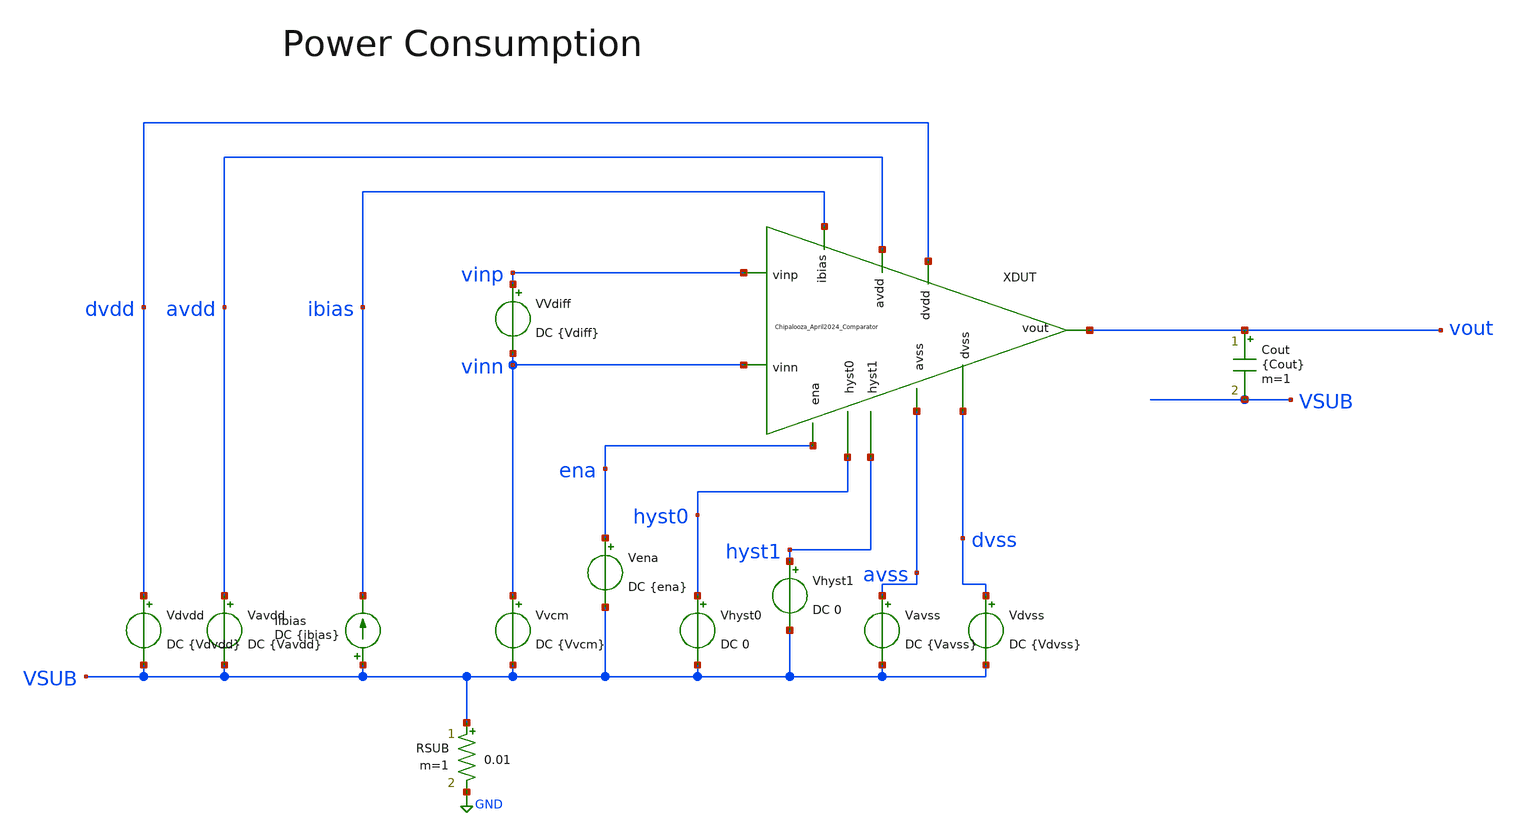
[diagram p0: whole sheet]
** sch_path: Chipalooza_April2024_Comparator/xschem/TB_powerConsumption.sch
**.subckt TB_powerConsumption
Vavdd avdd VSUB DC {Vavdd}
Cout vout VSUB {Cout} m=1
Vdvdd dvdd VSUB DC {Vdvdd}
Vvcm vinn VSUB DC {Vvcm}
Vena ena VSUB DC {ena}
Vhyst0 hyst0 VSUB DC 0
Vavss avss VSUB DC {Vavss}
Vdvss dvss VSUB DC {Vdvss}
RSUB VSUB GND 0.01 m=1
Iibias VSUB ibias DC {ibias}
VVdiff vinp vinn DC {Vdiff}
XDUT hyst0 hyst1 avdd vinp avss vinn dvdd dvss vout ibias ena Chipalooza_April2024_Comparator
Vhyst1 hyst1 VSUB DC 0
**** begin user architecture code

.control
.option savecurrents

.param vdvdd=1.8 vavdd=3.3 cout=1f
.param ibias=0.5u ena=1.8 Vhyst_0=1 Vhyst_1=1
.param vavss=0 vdvss=0
.param Vvcm=0 Vdiff=0.2


dc Vvcm 0 0.1 0.01
plot -(I(Vavdd) + I(Vdvdd)) + 500n

write TB_powerConsumption.raw

*quit

.endc


.lib $::SKYWATER_MODELS/sky130.lib.spice tt
**** end user architecture code
**.ends

* expanding   symbol:  Chipalooza_April2024_Comparator.sym # of pins=11
** sym_path: Chipalooza_April2024_Comparator/xschem/Chipalooza_April2024_Comparator.sym
** sch_path: Chipalooza_April2024_Comparator/xschem/Chipalooza_April2024_Comparator.sch
.subckt Chipalooza_April2024_Comparator hyst0 hyst1 avdd vinp avss vinn dvdd dvss vout ibias ena
*.ipin vinp
*.ipin vinn
*.ipin hyst0
*.ipin hyst1
*.ipin avdd
*.ipin avss
*.ipin dvdd
*.ipin dvss
*.opin vout
*.ipin ena
*.ipin ibias
XM29 SumOutBar SumOut dvdd dvdd sky130_fd_pr__pfet_01v8 L=1 W=2 nf=1 ad='int((nf+1)/2) * W/nf * 0.29'
+ as='int((nf+2)/2) * W/nf * 0.29' pd='2*int((nf+1)/2) * (W/nf + 0.29)' ps='2*int((nf+2)/2) * (W/nf + 0.29)'
+ nrd='0.29 / W' nrs='0.29 / W' sa=0 sb=0 sd=0 mult=2 m=2
XM30 SumOutBar SumOut avssi dvss sky130_fd_pr__nfet_01v8 L=1 W=2 nf=1 ad='int((nf+1)/2) * W/nf * 0.29'
+ as='int((nf+2)/2) * W/nf * 0.29' pd='2*int((nf+1)/2) * (W/nf + 0.29)' ps='2*int((nf+2)/2) * (W/nf + 0.29)'
+ nrd='0.29 / W' nrs='0.29 / W' sa=0 sb=0 sd=0 mult=2 m=2
XM25 net3 ibias avssi avss sky130_fd_pr__nfet_g5v0d10v5 L=1 W=1 nf=1 ad='int((nf+1)/2) * W/nf * 0.29'
+ as='int((nf+2)/2) * W/nf * 0.29' pd='2*int((nf+1)/2) * (W/nf + 0.29)' ps='2*int((nf+2)/2) * (W/nf + 0.29)'
+ nrd='0.29 / W' nrs='0.29 / W' sa=0 sb=0 sd=0 mult=2 m=2
C1 avss 0 2p m=1
XM38 avssi ena avss avss sky130_fd_pr__nfet_g5v0d10v5 L=1 W=32 nf=1 ad='int((nf+1)/2) * W/nf * 0.29'
+ as='int((nf+2)/2) * W/nf * 0.29' pd='2*int((nf+1)/2) * (W/nf + 0.29)' ps='2*int((nf+2)/2) * (W/nf + 0.29)'
+ nrd='0.29 / W' nrs='0.29 / W' sa=0 sb=0 sd=0 mult=8 m=8
XM39 net4 ibias avssi avss sky130_fd_pr__nfet_g5v0d10v5 L=1 W=3 nf=1 ad='int((nf+1)/2) * W/nf * 0.29'
+ as='int((nf+2)/2) * W/nf * 0.29' pd='2*int((nf+1)/2) * (W/nf + 0.29)' ps='2*int((nf+2)/2) * (W/nf + 0.29)'
+ nrd='0.29 / W' nrs='0.29 / W' sa=0 sb=0 sd=0 mult=2 m=2
XM16 vout SumOutBar dvdd dvdd sky130_fd_pr__pfet_01v8 L=1 W=2 nf=1 ad='int((nf+1)/2) * W/nf * 0.29' as='int((nf+2)/2) * W/nf * 0.29'
+ pd='2*int((nf+1)/2) * (W/nf + 0.29)' ps='2*int((nf+2)/2) * (W/nf + 0.29)' nrd='0.29 / W' nrs='0.29 / W'
+ sa=0 sb=0 sd=0 mult=2 m=2
XM18 vout SumOutBar avssi dvss sky130_fd_pr__nfet_01v8 L=1 W=2 nf=1 ad='int((nf+1)/2) * W/nf * 0.29'
+ as='int((nf+2)/2) * W/nf * 0.29' pd='2*int((nf+1)/2) * (W/nf + 0.29)' ps='2*int((nf+2)/2) * (W/nf + 0.29)'
+ nrd='0.29 / W' nrs='0.29 / W' sa=0 sb=0 sd=0 mult=2 m=2
XM4 SourceBias2 SourceBias2 avdd avdd sky130_fd_pr__pfet_g5v0d10v5 L=1 W=2 nf=1 ad='int((nf+1)/2) * W/nf * 0.29'
+ as='int((nf+2)/2) * W/nf * 0.29' pd='2*int((nf+1)/2) * (W/nf + 0.29)' ps='2*int((nf+2)/2) * (W/nf + 0.29)'
+ nrd='0.29 / W' nrs='0.29 / W' sa=0 sb=0 sd=0 mult=2 m=2
XM5 N1 SourceBias2 avdd avdd sky130_fd_pr__pfet_g5v0d10v5 L=1 W=2 nf=1 ad='int((nf+1)/2) * W/nf * 0.29'
+ as='int((nf+2)/2) * W/nf * 0.29' pd='2*int((nf+1)/2) * (W/nf + 0.29)' ps='2*int((nf+2)/2) * (W/nf + 0.29)'
+ nrd='0.29 / W' nrs='0.29 / W' sa=0 sb=0 sd=0 mult=2 m=2
XM6 N2 SourceBias2 avdd avdd sky130_fd_pr__pfet_g5v0d10v5 L=1 W=2 nf=1 ad='int((nf+1)/2) * W/nf * 0.29'
+ as='int((nf+2)/2) * W/nf * 0.29' pd='2*int((nf+1)/2) * (W/nf + 0.29)' ps='2*int((nf+2)/2) * (W/nf + 0.29)'
+ nrd='0.29 / W' nrs='0.29 / W' sa=0 sb=0 sd=0 mult=2 m=2
XM7 SumOut Bias1 N2 avdd sky130_fd_pr__pfet_g5v0d10v5 L=1 W=2 nf=1 ad='int((nf+1)/2) * W/nf * 0.29' as='int((nf+2)/2) * W/nf * 0.29'
+ pd='2*int((nf+1)/2) * (W/nf + 0.29)' ps='2*int((nf+2)/2) * (W/nf + 0.29)' nrd='0.29 / W' nrs='0.29 / W'
+ sa=0 sb=0 sd=0 mult=2 m=2
XM8 Sum Bias1 N1 avdd sky130_fd_pr__pfet_g5v0d10v5 L=1 W=2 nf=1 ad='int((nf+1)/2) * W/nf * 0.29' as='int((nf+2)/2) * W/nf * 0.29'
+ pd='2*int((nf+1)/2) * (W/nf + 0.29)' ps='2*int((nf+2)/2) * (W/nf + 0.29)' nrd='0.29 / W' nrs='0.29 / W'
+ sa=0 sb=0 sd=0 mult=2 m=2
XM9 SumOut Bias2 P2 avss sky130_fd_pr__nfet_g5v0d10v5 L=1 W=2 nf=1 ad='int((nf+1)/2) * W/nf * 0.29' as='int((nf+2)/2) * W/nf * 0.29'
+ pd='2*int((nf+1)/2) * (W/nf + 0.29)' ps='2*int((nf+2)/2) * (W/nf + 0.29)' nrd='0.29 / W' nrs='0.29 / W'
+ sa=0 sb=0 sd=0 mult=2 m=2
XM10 Sum Bias2 P1 avss sky130_fd_pr__nfet_g5v0d10v5 L=1 W=2 nf=1 ad='int((nf+1)/2) * W/nf * 0.29' as='int((nf+2)/2) * W/nf * 0.29'
+ pd='2*int((nf+1)/2) * (W/nf + 0.29)' ps='2*int((nf+2)/2) * (W/nf + 0.29)' nrd='0.29 / W' nrs='0.29 / W'
+ sa=0 sb=0 sd=0 mult=2 m=2
XM11 P2 Sum avssi avss sky130_fd_pr__nfet_g5v0d10v5 L=1 W=2 nf=1 ad='int((nf+1)/2) * W/nf * 0.29' as='int((nf+2)/2) * W/nf * 0.29'
+ pd='2*int((nf+1)/2) * (W/nf + 0.29)' ps='2*int((nf+2)/2) * (W/nf + 0.29)' nrd='0.29 / W' nrs='0.29 / W'
+ sa=0 sb=0 sd=0 mult=2 m=2
XM12 P1 Sum avssi avss sky130_fd_pr__nfet_g5v0d10v5 L=1 W=2 nf=1 ad='int((nf+1)/2) * W/nf * 0.29' as='int((nf+2)/2) * W/nf * 0.29'
+ pd='2*int((nf+1)/2) * (W/nf + 0.29)' ps='2*int((nf+2)/2) * (W/nf + 0.29)' nrd='0.29 / W' nrs='0.29 / W'
+ sa=0 sb=0 sd=0 mult=2 m=2
XM2 P2 vinn psource_input avdd sky130_fd_pr__pfet_g5v0d10v5 L=1 W=4 nf=1 ad='int((nf+1)/2) * W/nf * 0.29'
+ as='int((nf+2)/2) * W/nf * 0.29' pd='2*int((nf+1)/2) * (W/nf + 0.29)' ps='2*int((nf+2)/2) * (W/nf + 0.29)'
+ nrd='0.29 / W' nrs='0.29 / W' sa=0 sb=0 sd=0 mult=2 m=2
XM3 P1 vinp psource_input avdd sky130_fd_pr__pfet_g5v0d10v5 L=1 W=4 nf=1 ad='int((nf+1)/2) * W/nf * 0.29'
+ as='int((nf+2)/2) * W/nf * 0.29' pd='2*int((nf+1)/2) * (W/nf + 0.29)' ps='2*int((nf+2)/2) * (W/nf + 0.29)'
+ nrd='0.29 / W' nrs='0.29 / W' sa=0 sb=0 sd=0 mult=2 m=2
XM14 psource_input net5 avdd avdd sky130_fd_pr__pfet_g5v0d10v5 L=1 W=12 nf=1 ad='int((nf+1)/2) * W/nf * 0.29'
+ as='int((nf+2)/2) * W/nf * 0.29' pd='2*int((nf+1)/2) * (W/nf + 0.29)' ps='2*int((nf+2)/2) * (W/nf + 0.29)'
+ nrd='0.29 / W' nrs='0.29 / W' sa=0 sb=0 sd=0 mult=4 m=4
XM15 net5 net5 avdd avdd sky130_fd_pr__pfet_g5v0d10v5 L=1 W=8 nf=1 ad='int((nf+1)/2) * W/nf * 0.29' as='int((nf+2)/2) * W/nf * 0.29'
+ pd='2*int((nf+1)/2) * (W/nf + 0.29)' ps='2*int((nf+2)/2) * (W/nf + 0.29)' nrd='0.29 / W' nrs='0.29 / W'
+ sa=0 sb=0 sd=0 mult=2 m=2
XM17 nbias_tail net10 psource_input avdd sky130_fd_pr__pfet_g5v0d10v5 L=1 W=8 nf=1 ad='int((nf+1)/2) * W/nf * 0.29'
+ as='int((nf+2)/2) * W/nf * 0.29' pd='2*int((nf+1)/2) * (W/nf + 0.29)' ps='2*int((nf+2)/2) * (W/nf + 0.29)'
+ nrd='0.29 / W' nrs='0.29 / W' sa=0 sb=0 sd=0 mult=2 m=2
XM20 N1 vinp SourceBias0 avss sky130_fd_pr__nfet_g5v0d10v5 L=4 W=16 nf=1 ad='int((nf+1)/2) * W/nf * 0.29'
+ as='int((nf+2)/2) * W/nf * 0.29' pd='2*int((nf+1)/2) * (W/nf + 0.29)' ps='2*int((nf+2)/2) * (W/nf + 0.29)'
+ nrd='0.29 / W' nrs='0.29 / W' sa=0 sb=0 sd=0 mult=2 m=2
XM21 N2 vinn SourceBias0 avss sky130_fd_pr__nfet_g5v0d10v5 L=4 W=16 nf=1 ad='int((nf+1)/2) * W/nf * 0.29'
+ as='int((nf+2)/2) * W/nf * 0.29' pd='2*int((nf+1)/2) * (W/nf + 0.29)' ps='2*int((nf+2)/2) * (W/nf + 0.29)'
+ nrd='0.29 / W' nrs='0.29 / W' sa=0 sb=0 sd=0 mult=2 m=2
XM22 SourceBias0 nbias_tail avssi avss sky130_fd_pr__nfet_g5v0d10v5 L=1 W=12 nf=1 ad='int((nf+1)/2) * W/nf * 0.29'
+ as='int((nf+2)/2) * W/nf * 0.29' pd='2*int((nf+1)/2) * (W/nf + 0.29)' ps='2*int((nf+2)/2) * (W/nf + 0.29)'
+ nrd='0.29 / W' nrs='0.29 / W' sa=0 sb=0 sd=0 mult=4 m=4
XM23 nbias_tail nbias_tail avssi avss sky130_fd_pr__nfet_g5v0d10v5 L=1 W=12 nf=1 ad='int((nf+1)/2) * W/nf * 0.29'
+ as='int((nf+2)/2) * W/nf * 0.29' pd='2*int((nf+1)/2) * (W/nf + 0.29)' ps='2*int((nf+2)/2) * (W/nf + 0.29)'
+ nrd='0.29 / W' nrs='0.29 / W' sa=0 sb=0 sd=0 mult=2 m=2
XM28 net5 Bias5 SourceBias0 avss sky130_fd_pr__nfet_g5v0d10v5 L=1 W=4 nf=1 ad='int((nf+1)/2) * W/nf * 0.29'
+ as='int((nf+2)/2) * W/nf * 0.29' pd='2*int((nf+1)/2) * (W/nf + 0.29)' ps='2*int((nf+2)/2) * (W/nf + 0.29)'
+ nrd='0.29 / W' nrs='0.29 / W' sa=0 sb=0 sd=0 mult=2 m=2
XM45 SourceBias1 ibias avssi avss sky130_fd_pr__nfet_g5v0d10v5 L=1 W=3 nf=1 ad='int((nf+1)/2) * W/nf * 0.29'
+ as='int((nf+2)/2) * W/nf * 0.29' pd='2*int((nf+1)/2) * (W/nf + 0.29)' ps='2*int((nf+2)/2) * (W/nf + 0.29)'
+ nrd='0.29 / W' nrs='0.29 / W' sa=0 sb=0 sd=0 mult=2 m=2
XM46 SourceBias1 SourceBias1 avdd avdd sky130_fd_pr__pfet_g5v0d10v5 L=1 W=12 nf=1 ad='int((nf+1)/2) * W/nf * 0.29'
+ as='int((nf+2)/2) * W/nf * 0.29' pd='2*int((nf+1)/2) * (W/nf + 0.29)' ps='2*int((nf+2)/2) * (W/nf + 0.29)'
+ nrd='0.29 / W' nrs='0.29 / W' sa=0 sb=0 sd=0 mult=4 m=4
XM47 psource_input SourceBias1 avdd avdd sky130_fd_pr__pfet_g5v0d10v5 L=1 W=12 nf=1 ad='int((nf+1)/2) * W/nf * 0.29'
+ as='int((nf+2)/2) * W/nf * 0.29' pd='2*int((nf+1)/2) * (W/nf + 0.29)' ps='2*int((nf+2)/2) * (W/nf + 0.29)'
+ nrd='0.29 / W' nrs='0.29 / W' sa=0 sb=0 sd=0 mult=4 m=4
XM48 SourceBias2 ibias avssi avss sky130_fd_pr__nfet_g5v0d10v5 L=1 W=6 nf=1 ad='int((nf+1)/2) * W/nf * 0.29'
+ as='int((nf+2)/2) * W/nf * 0.29' pd='2*int((nf+1)/2) * (W/nf + 0.29)' ps='2*int((nf+2)/2) * (W/nf + 0.29)'
+ nrd='0.29 / W' nrs='0.29 / W' sa=0 sb=0 sd=0 mult=2 m=2
XM65 SourceBias3 ibias avssi avss sky130_fd_pr__nfet_g5v0d10v5 L=1 W=1 nf=1 ad='int((nf+1)/2) * W/nf * 0.29'
+ as='int((nf+2)/2) * W/nf * 0.29' pd='2*int((nf+1)/2) * (W/nf + 0.29)' ps='2*int((nf+2)/2) * (W/nf + 0.29)'
+ nrd='0.29 / W' nrs='0.29 / W' sa=0 sb=0 sd=0 mult=2 m=2
XM76 Bias1 ibias avssi avss sky130_fd_pr__nfet_g5v0d10v5 L=1 W=3 nf=1 ad='int((nf+1)/2) * W/nf * 0.29'
+ as='int((nf+2)/2) * W/nf * 0.29' pd='2*int((nf+1)/2) * (W/nf + 0.29)' ps='2*int((nf+2)/2) * (W/nf + 0.29)'
+ nrd='0.29 / W' nrs='0.29 / W' sa=0 sb=0 sd=0 mult=2 m=2
XM77 SourceBias5 ibias avssi avss sky130_fd_pr__nfet_g5v0d10v5 L=1 W=3 nf=1 ad='int((nf+1)/2) * W/nf * 0.29'
+ as='int((nf+2)/2) * W/nf * 0.29' pd='2*int((nf+1)/2) * (W/nf + 0.29)' ps='2*int((nf+2)/2) * (W/nf + 0.29)'
+ nrd='0.29 / W' nrs='0.29 / W' sa=0 sb=0 sd=0 mult=2 m=2
XM78 SourceBias6 ibias avssi avss sky130_fd_pr__nfet_g5v0d10v5 L=1 W=3 nf=1 ad='int((nf+1)/2) * W/nf * 0.29'
+ as='int((nf+2)/2) * W/nf * 0.29' pd='2*int((nf+1)/2) * (W/nf + 0.29)' ps='2*int((nf+2)/2) * (W/nf + 0.29)'
+ nrd='0.29 / W' nrs='0.29 / W' sa=0 sb=0 sd=0 mult=2 m=2
XM79 SourceBias7 ibias avssi avss sky130_fd_pr__nfet_g5v0d10v5 L=1 W=3 nf=1 ad='int((nf+1)/2) * W/nf * 0.29'
+ as='int((nf+2)/2) * W/nf * 0.29' pd='2*int((nf+1)/2) * (W/nf + 0.29)' ps='2*int((nf+2)/2) * (W/nf + 0.29)'
+ nrd='0.29 / W' nrs='0.29 / W' sa=0 sb=0 sd=0 mult=2 m=2
XM81 Bias5 ibias avssi avss sky130_fd_pr__nfet_g5v0d10v5 L=1 W=3 nf=1 ad='int((nf+1)/2) * W/nf * 0.29'
+ as='int((nf+2)/2) * W/nf * 0.29' pd='2*int((nf+1)/2) * (W/nf + 0.29)' ps='2*int((nf+2)/2) * (W/nf + 0.29)'
+ nrd='0.29 / W' nrs='0.29 / W' sa=0 sb=0 sd=0 mult=2 m=2
XM54 M55Source M55Drain avssi avss sky130_fd_pr__nfet_g5v0d10v5 L=1.5 W=6 nf=1 ad='int((nf+1)/2) * W/nf * 0.29'
+ as='int((nf+2)/2) * W/nf * 0.29' pd='2*int((nf+1)/2) * (W/nf + 0.29)' ps='2*int((nf+2)/2) * (W/nf + 0.29)'
+ nrd='0.29 / W' nrs='0.29 / W' sa=0 sb=0 sd=0 mult=2 m=2
XM55 M55Drain Bias2 M55Source avss sky130_fd_pr__nfet_g5v0d10v5 L=1 W=9 nf=1 ad='int((nf+1)/2) * W/nf * 0.29'
+ as='int((nf+2)/2) * W/nf * 0.29' pd='2*int((nf+1)/2) * (W/nf + 0.29)' ps='2*int((nf+2)/2) * (W/nf + 0.29)'
+ nrd='0.29 / W' nrs='0.29 / W' sa=0 sb=0 sd=0 mult=2 m=2
XM56 Bias2 Bias2 avssi avss sky130_fd_pr__nfet_g5v0d10v5 L=2 W=0.5 nf=1 ad='int((nf+1)/2) * W/nf * 0.29'
+ as='int((nf+2)/2) * W/nf * 0.29' pd='2*int((nf+1)/2) * (W/nf + 0.29)' ps='2*int((nf+2)/2) * (W/nf + 0.29)'
+ nrd='0.29 / W' nrs='0.29 / W' sa=0 sb=0 sd=0 mult=1 m=1
XM51 net6 net7 avdd avdd sky130_fd_pr__pfet_g5v0d10v5 L=2 W=20 nf=1 ad='int((nf+1)/2) * W/nf * 0.29'
+ as='int((nf+2)/2) * W/nf * 0.29' pd='2*int((nf+1)/2) * (W/nf + 0.29)' ps='2*int((nf+2)/2) * (W/nf + 0.29)'
+ nrd='0.29 / W' nrs='0.29 / W' sa=0 sb=0 sd=0 mult=2 m=2
XM49 net7 net7 avdd avdd sky130_fd_pr__pfet_g5v0d10v5 L=2 W=10 nf=1 ad='int((nf+1)/2) * W/nf * 0.29'
+ as='int((nf+2)/2) * W/nf * 0.29' pd='2*int((nf+1)/2) * (W/nf + 0.29)' ps='2*int((nf+2)/2) * (W/nf + 0.29)'
+ nrd='0.29 / W' nrs='0.29 / W' sa=0 sb=0 sd=0 mult=2 m=2
XM50 SourceBias4 SourceBias4 net7 avdd sky130_fd_pr__pfet_g5v0d10v5 L=1 W=10 nf=1 ad='int((nf+1)/2) * W/nf * 0.29'
+ as='int((nf+2)/2) * W/nf * 0.29' pd='2*int((nf+1)/2) * (W/nf + 0.29)' ps='2*int((nf+2)/2) * (W/nf + 0.29)'
+ nrd='0.29 / W' nrs='0.29 / W' sa=0 sb=0 sd=0 mult=2 m=2
XM52 avssi SourceBias4 net6 avdd sky130_fd_pr__pfet_g5v0d10v5 L=1 W=1 nf=1 ad='int((nf+1)/2) * W/nf * 0.29'
+ as='int((nf+2)/2) * W/nf * 0.29' pd='2*int((nf+1)/2) * (W/nf + 0.29)' ps='2*int((nf+2)/2) * (W/nf + 0.29)'
+ nrd='0.29 / W' nrs='0.29 / W' sa=0 sb=0 sd=0 mult=2 m=2
XM53 Bias1 Bias1 net6 avdd sky130_fd_pr__pfet_g5v0d10v5 L=1 W=10 nf=1 ad='int((nf+1)/2) * W/nf * 0.29'
+ as='int((nf+2)/2) * W/nf * 0.29' pd='2*int((nf+1)/2) * (W/nf + 0.29)' ps='2*int((nf+2)/2) * (W/nf + 0.29)'
+ nrd='0.29 / W' nrs='0.29 / W' sa=0 sb=0 sd=0 mult=2 m=2
XM66 net8 net9 avdd avdd sky130_fd_pr__pfet_g5v0d10v5 L=2 W=20 nf=1 ad='int((nf+1)/2) * W/nf * 0.29'
+ as='int((nf+2)/2) * W/nf * 0.29' pd='2*int((nf+1)/2) * (W/nf + 0.29)' ps='2*int((nf+2)/2) * (W/nf + 0.29)'
+ nrd='0.29 / W' nrs='0.29 / W' sa=0 sb=0 sd=0 mult=2 m=2
XM67 net9 net9 avdd avdd sky130_fd_pr__pfet_g5v0d10v5 L=2 W=20 nf=1 ad='int((nf+1)/2) * W/nf * 0.29'
+ as='int((nf+2)/2) * W/nf * 0.29' pd='2*int((nf+1)/2) * (W/nf + 0.29)' ps='2*int((nf+2)/2) * (W/nf + 0.29)'
+ nrd='0.29 / W' nrs='0.29 / W' sa=0 sb=0 sd=0 mult=2 m=2
XM68 SourceBias7 SourceBias7 net9 avdd sky130_fd_pr__pfet_g5v0d10v5 L=1 W=10 nf=1 ad='int((nf+1)/2) * W/nf * 0.29'
+ as='int((nf+2)/2) * W/nf * 0.29' pd='2*int((nf+1)/2) * (W/nf + 0.29)' ps='2*int((nf+2)/2) * (W/nf + 0.29)'
+ nrd='0.29 / W' nrs='0.29 / W' sa=0 sb=0 sd=0 mult=2 m=2
XM69 avssi SourceBias7 net8 avdd sky130_fd_pr__pfet_g5v0d10v5 L=1 W=1 nf=1 ad='int((nf+1)/2) * W/nf * 0.29'
+ as='int((nf+2)/2) * W/nf * 0.29' pd='2*int((nf+1)/2) * (W/nf + 0.29)' ps='2*int((nf+2)/2) * (W/nf + 0.29)'
+ nrd='0.29 / W' nrs='0.29 / W' sa=0 sb=0 sd=0 mult=2 m=2
XM70 Bias5 Bias5 net8 avdd sky130_fd_pr__pfet_g5v0d10v5 L=1 W=5 nf=1 ad='int((nf+1)/2) * W/nf * 0.29'
+ as='int((nf+2)/2) * W/nf * 0.29' pd='2*int((nf+1)/2) * (W/nf + 0.29)' ps='2*int((nf+2)/2) * (W/nf + 0.29)'
+ nrd='0.29 / W' nrs='0.29 / W' sa=0 sb=0 sd=0 mult=2 m=2
XM72 SourceBias5 SourceBias5 avdd avdd sky130_fd_pr__pfet_g5v0d10v5 L=1 W=12 nf=1 ad='int((nf+1)/2) * W/nf * 0.29'
+ as='int((nf+2)/2) * W/nf * 0.29' pd='2*int((nf+1)/2) * (W/nf + 0.29)' ps='2*int((nf+2)/2) * (W/nf + 0.29)'
+ nrd='0.29 / W' nrs='0.29 / W' sa=0 sb=0 sd=0 mult=4 m=4
XM73 M55Drain SourceBias5 avdd avdd sky130_fd_pr__pfet_g5v0d10v5 L=1 W=12 nf=1 ad='int((nf+1)/2) * W/nf * 0.29'
+ as='int((nf+2)/2) * W/nf * 0.29' pd='2*int((nf+1)/2) * (W/nf + 0.29)' ps='2*int((nf+2)/2) * (W/nf + 0.29)'
+ nrd='0.29 / W' nrs='0.29 / W' sa=0 sb=0 sd=0 mult=4 m=4
XM74 SourceBias6 SourceBias6 avdd avdd sky130_fd_pr__pfet_g5v0d10v5 L=1 W=12 nf=1 ad='int((nf+1)/2) * W/nf * 0.29'
+ as='int((nf+2)/2) * W/nf * 0.29' pd='2*int((nf+1)/2) * (W/nf + 0.29)' ps='2*int((nf+2)/2) * (W/nf + 0.29)'
+ nrd='0.29 / W' nrs='0.29 / W' sa=0 sb=0 sd=0 mult=4 m=4
XM75 Bias2 SourceBias6 avdd avdd sky130_fd_pr__pfet_g5v0d10v5 L=1 W=12 nf=1 ad='int((nf+1)/2) * W/nf * 0.29'
+ as='int((nf+2)/2) * W/nf * 0.29' pd='2*int((nf+1)/2) * (W/nf + 0.29)' ps='2*int((nf+2)/2) * (W/nf + 0.29)'
+ nrd='0.29 / W' nrs='0.29 / W' sa=0 sb=0 sd=0 mult=4 m=4
XM1 SourceBias0 ibias avssi avss sky130_fd_pr__nfet_g5v0d10v5 L=1 W=3 nf=1 ad='int((nf+1)/2) * W/nf * 0.29'
+ as='int((nf+2)/2) * W/nf * 0.29' pd='2*int((nf+1)/2) * (W/nf + 0.29)' ps='2*int((nf+2)/2) * (W/nf + 0.29)'
+ nrd='0.29 / W' nrs='0.29 / W' sa=0 sb=0 sd=0 mult=2 m=2
XM31 net1 hyst0 net3 avss sky130_fd_pr__nfet_01v8 L=1 W=1 nf=1 ad='int((1 + 1)/2) * 1 / 1 * 0.29' as='int((1 + 2)/2) * 1 / 1 * 0.29'
+ pd='2*int((1 + 1)/2) * (1 / 1 + 0.29)' ps='2*int((1 + 2)/2) * (1 / 1 + 0.29)' nrd='0.29 / 1 ' nrs='0.29 / 1 '
+ sa=0 sb=0 sd=0 mult=2 m=2
XM32 net1 hyst1 net4 avss sky130_fd_pr__nfet_01v8 L=1 W=3 nf=1 ad='int((1 + 1)/2) * 3 / 1 * 0.29' as='int((1 + 2)/2) * 3 / 1 * 0.29'
+ pd='2*int((1 + 1)/2) * (3 / 1 + 0.29)' ps='2*int((1 + 2)/2) * (3 / 1 + 0.29)' nrd='0.29 / 3 ' nrs='0.29 / 3 '
+ sa=0 sb=0 sd=0 mult=2 m=2
XM19 N1 SumOut net1 avss sky130_fd_pr__nfet_g5v0d10v5 L=1 W=2 nf=1 ad='int((nf+1)/2) * W/nf * 0.29' as='int((nf+2)/2) * W/nf * 0.29'
+ pd='2*int((nf+1)/2) * (W/nf + 0.29)' ps='2*int((nf+2)/2) * (W/nf + 0.29)' nrd='0.29 / W' nrs='0.29 / W'
+ sa=0 sb=0 sd=0 mult=2 m=2
XM24 N2 SumOutBar net1 avss sky130_fd_pr__nfet_g5v0d10v5 L=1 W=2 nf=1 ad='int((nf+1)/2) * W/nf * 0.29'
+ as='int((nf+2)/2) * W/nf * 0.29' pd='2*int((nf+1)/2) * (W/nf + 0.29)' ps='2*int((nf+2)/2) * (W/nf + 0.29)'
+ nrd='0.29 / W' nrs='0.29 / W' sa=0 sb=0 sd=0 mult=2 m=2
XM26 ibias ibias avssi avss sky130_fd_pr__nfet_g5v0d10v5 L=1 W=3 nf=1 ad='int((nf+1)/2) * W/nf * 0.29'
+ as='int((nf+2)/2) * W/nf * 0.29' pd='2*int((nf+1)/2) * (W/nf + 0.29)' ps='2*int((nf+2)/2) * (W/nf + 0.29)'
+ nrd='0.29 / W' nrs='0.29 / W' sa=0 sb=0 sd=0 mult=2 m=2
XM27 net2 ibias avssi avss sky130_fd_pr__nfet_g5v0d10v5 L=1 W=3 nf=1 ad='int((nf+1)/2) * W/nf * 0.29'
+ as='int((nf+2)/2) * W/nf * 0.29' pd='2*int((nf+1)/2) * (W/nf + 0.29)' ps='2*int((nf+2)/2) * (W/nf + 0.29)'
+ nrd='0.29 / W' nrs='0.29 / W' sa=0 sb=0 sd=0 mult=2 m=2
XM33 net2 net2 avdd avdd sky130_fd_pr__pfet_g5v0d10v5 L=1 W=3 nf=1 ad='int((nf+1)/2) * W/nf * 0.29' as='int((nf+2)/2) * W/nf * 0.29'
+ pd='2*int((nf+1)/2) * (W/nf + 0.29)' ps='2*int((nf+2)/2) * (W/nf + 0.29)' nrd='0.29 / W' nrs='0.29 / W'
+ sa=0 sb=0 sd=0 mult=2 m=2
XM34 avss net2 avdd avdd sky130_fd_pr__pfet_g5v0d10v5 L=1 W=3 nf=1 ad='int((nf+1)/2) * W/nf * 0.29' as='int((nf+2)/2) * W/nf * 0.29'
+ pd='2*int((nf+1)/2) * (W/nf + 0.29)' ps='2*int((nf+2)/2) * (W/nf + 0.29)' nrd='0.29 / W' nrs='0.29 / W'
+ sa=0 sb=0 sd=0 mult=2 m=2
XM63 net10 net10 avdd avdd sky130_fd_pr__pfet_g5v0d10v5 L=5 W=3 nf=1 ad='int((nf+1)/2) * W/nf * 0.29'
+ as='int((nf+2)/2) * W/nf * 0.29' pd='2*int((nf+1)/2) * (W/nf + 0.29)' ps='2*int((nf+2)/2) * (W/nf + 0.29)'
+ nrd='0.29 / W' nrs='0.29 / W' sa=0 sb=0 sd=0 mult=1 m=1
XM62 avdd Bias4 SourceBias3 avss sky130_fd_pr__nfet_g5v0d10v5 L=1 W=4 nf=1 ad='int((nf+1)/2) * W/nf * 0.29'
+ as='int((nf+2)/2) * W/nf * 0.29' pd='2*int((nf+1)/2) * (W/nf + 0.29)' ps='2*int((nf+2)/2) * (W/nf + 0.29)'
+ nrd='0.29 / W' nrs='0.29 / W' sa=0 sb=0 sd=0 mult=2 m=2
XM64 net10 Bias4 SourceBias3 avss sky130_fd_pr__nfet_g5v0d10v5 L=1 W=4 nf=1 ad='int((nf+1)/2) * W/nf * 0.29'
+ as='int((nf+2)/2) * W/nf * 0.29' pd='2*int((nf+1)/2) * (W/nf + 0.29)' ps='2*int((nf+2)/2) * (W/nf + 0.29)'
+ nrd='0.29 / W' nrs='0.29 / W' sa=0 sb=0 sd=0 mult=2 m=2
XM57 net11 net12 avdd avdd sky130_fd_pr__pfet_g5v0d10v5 L=2 W=20 nf=1 ad='int((nf+1)/2) * W/nf * 0.29'
+ as='int((nf+2)/2) * W/nf * 0.29' pd='2*int((nf+1)/2) * (W/nf + 0.29)' ps='2*int((nf+2)/2) * (W/nf + 0.29)'
+ nrd='0.29 / W' nrs='0.29 / W' sa=0 sb=0 sd=0 mult=2 m=2
XM58 net12 net12 avdd avdd sky130_fd_pr__pfet_g5v0d10v5 L=2 W=10 nf=1 ad='int((nf+1)/2) * W/nf * 0.29'
+ as='int((nf+2)/2) * W/nf * 0.29' pd='2*int((nf+1)/2) * (W/nf + 0.29)' ps='2*int((nf+2)/2) * (W/nf + 0.29)'
+ nrd='0.29 / W' nrs='0.29 / W' sa=0 sb=0 sd=0 mult=2 m=2
XM59 SourceBias10 SourceBias10 net12 avdd sky130_fd_pr__pfet_g5v0d10v5 L=1 W=10 nf=1 ad='int((nf+1)/2) * W/nf * 0.29'
+ as='int((nf+2)/2) * W/nf * 0.29' pd='2*int((nf+1)/2) * (W/nf + 0.29)' ps='2*int((nf+2)/2) * (W/nf + 0.29)'
+ nrd='0.29 / W' nrs='0.29 / W' sa=0 sb=0 sd=0 mult=2 m=2
XM60 avss SourceBias10 net11 avdd sky130_fd_pr__pfet_g5v0d10v5 L=1 W=1 nf=1 ad='int((nf+1)/2) * W/nf * 0.29'
+ as='int((nf+2)/2) * W/nf * 0.29' pd='2*int((nf+1)/2) * (W/nf + 0.29)' ps='2*int((nf+2)/2) * (W/nf + 0.29)'
+ nrd='0.29 / W' nrs='0.29 / W' sa=0 sb=0 sd=0 mult=2 m=2
XM61 net13 net13 net11 avdd sky130_fd_pr__pfet_g5v0d10v5 L=1 W=5 nf=1 ad='int((nf+1)/2) * W/nf * 0.29'
+ as='int((nf+2)/2) * W/nf * 0.29' pd='2*int((nf+1)/2) * (W/nf + 0.29)' ps='2*int((nf+2)/2) * (W/nf + 0.29)'
+ nrd='0.29 / W' nrs='0.29 / W' sa=0 sb=0 sd=0 mult=2 m=2
XM13 avss ibias avss avss sky130_fd_pr__nfet_g5v0d10v5 L=1 W=3 nf=1 ad='int((nf+1)/2) * W/nf * 0.29'
+ as='int((nf+2)/2) * W/nf * 0.29' pd='2*int((nf+1)/2) * (W/nf + 0.29)' ps='2*int((nf+2)/2) * (W/nf + 0.29)'
+ nrd='0.29 / W' nrs='0.29 / W' sa=0 sb=0 sd=0 mult=2 m=2
XM35 SourceBias10 ibias avss avss sky130_fd_pr__nfet_g5v0d10v5 L=1 W=3 nf=1 ad='int((nf+1)/2) * W/nf * 0.29'
+ as='int((nf+2)/2) * W/nf * 0.29' pd='2*int((nf+1)/2) * (W/nf + 0.29)' ps='2*int((nf+2)/2) * (W/nf + 0.29)'
+ nrd='0.29 / W' nrs='0.29 / W' sa=0 sb=0 sd=0 mult=2 m=2
V1 Bias4 avss 1.5
V2 Bias5 avss 3
.ends

.GLOBAL GND
.end
